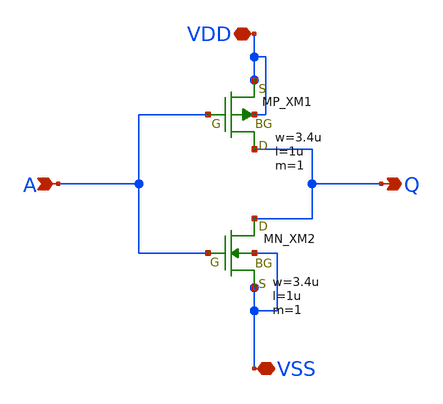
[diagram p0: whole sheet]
** sch_path: schematic/20250924_OSS_Workshop/Qdai/inverter_MUX_01/inv_hayashi.sch
**.subckt inv_hayashi VDD VSS A Q
*.iopin VDD
*.iopin VSS
*.ipin A
*.opin Q
XM2 Q A VSS VSS NMOS w=3.4u l=1u as=0 ad=0 ps=0 pd=0 nrd=0 nrs=0 m=1
XM1 Q A VDD VDD PMOS w=3.4u l=1u as=0 ad=0 ps=0 pd=0 nrd=0 nrs=0 m=1
**.ends
.end
